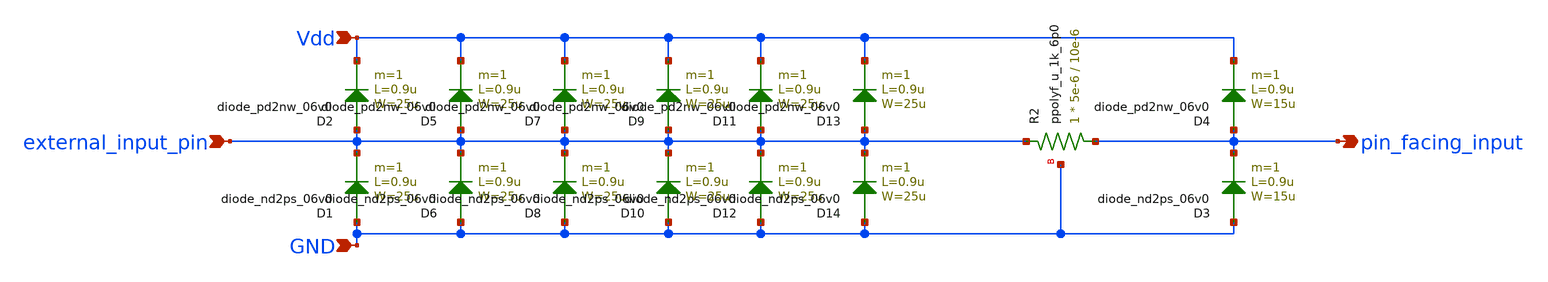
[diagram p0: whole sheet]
** sch_path: MG_ESD_protection/MG_ESD_protection.sch
**.subckt MG_ESD_protection external_input_pin Vdd GND pin_facing_input
*.ipin external_input_pin
*.ipin Vdd
*.ipin GND
*.opin pin_facing_input
D2 external_input_pin Vdd diode_pd2nw_06v0 area='25u * 0.9u ' pj='2*25u + 2*0.9u ' m=1
XR2 pin_facing_input external_input_pin GND ppolyf_u_1k_6p0 r_width=5e-6 r_length=10e-6 m=1
D1 GND external_input_pin diode_nd2ps_06v0 area='25u * 0.9u ' pj='2*25u + 2*0.9u ' m=1
D3 GND pin_facing_input diode_nd2ps_06v0 area='15u * 0.9u ' pj='2*15u + 2*0.9u ' m=1
D4 pin_facing_input Vdd diode_pd2nw_06v0 area='15u * 0.9u ' pj='2*15u + 2*0.9u ' m=1
D5 external_input_pin Vdd diode_pd2nw_06v0 area='25u * 0.9u ' pj='2*25u + 2*0.9u ' m=1
D6 GND external_input_pin diode_nd2ps_06v0 area='25u * 0.9u ' pj='2*25u + 2*0.9u ' m=1
D11 external_input_pin Vdd diode_pd2nw_06v0 area='25u * 0.9u ' pj='2*25u + 2*0.9u ' m=1
D12 GND external_input_pin diode_nd2ps_06v0 area='25u * 0.9u ' pj='2*25u + 2*0.9u ' m=1
D13 external_input_pin Vdd diode_pd2nw_06v0 area='25u * 0.9u ' pj='2*25u + 2*0.9u ' m=1
D14 GND external_input_pin diode_nd2ps_06v0 area='25u * 0.9u ' pj='2*25u + 2*0.9u ' m=1
D7 external_input_pin Vdd diode_pd2nw_06v0 area='25u * 0.9u ' pj='2*25u + 2*0.9u ' m=1
D8 GND external_input_pin diode_nd2ps_06v0 area='25u * 0.9u ' pj='2*25u + 2*0.9u ' m=1
D9 external_input_pin Vdd diode_pd2nw_06v0 area='25u * 0.9u ' pj='2*25u + 2*0.9u ' m=1
D10 GND external_input_pin diode_nd2ps_06v0 area='25u * 0.9u ' pj='2*25u + 2*0.9u ' m=1
**.ends
.end
